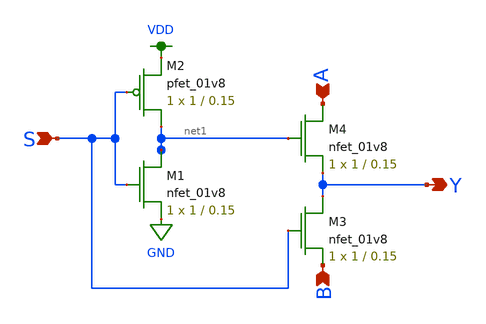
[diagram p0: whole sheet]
** sch_path: schematics/mux.sch
**.subckt mux S A Y B
*.ipin S
*.ipin A
*.opin Y
*.ipin B
XM1 net1 S GND GND sky130_fd_pr__nfet_01v8 L=0.15 W=1 nf=1 ad='int((nf+1)/2) * W/nf * 0.29' as='int((nf+2)/2) * W/nf * 0.29'
+ pd='2*int((nf+1)/2) * (W/nf + 0.29)' ps='2*int((nf+2)/2) * (W/nf + 0.29)' nrd='0.29 / W' nrs='0.29 / W'
+ sa=0 sb=0 sd=0 mult=1 m=1
XM2 net1 S VDD VDD sky130_fd_pr__pfet_01v8 L=0.15 W=1 nf=1 ad='int((nf+1)/2) * W/nf * 0.29' as='int((nf+2)/2) * W/nf * 0.29'
+ pd='2*int((nf+1)/2) * (W/nf + 0.29)' ps='2*int((nf+2)/2) * (W/nf + 0.29)' nrd='0.29 / W' nrs='0.29 / W'
+ sa=0 sb=0 sd=0 mult=1 m=1
XM3 Y S B GND sky130_fd_pr__nfet_01v8 L=0.15 W=1 nf=1 ad='int((nf+1)/2) * W/nf * 0.29' as='int((nf+2)/2) * W/nf * 0.29'
+ pd='2*int((nf+1)/2) * (W/nf + 0.29)' ps='2*int((nf+2)/2) * (W/nf + 0.29)' nrd='0.29 / W' nrs='0.29 / W'
+ sa=0 sb=0 sd=0 mult=1 m=1
XM4 A net1 Y GND sky130_fd_pr__nfet_01v8 L=0.15 W=1 nf=1 ad='int((nf+1)/2) * W/nf * 0.29' as='int((nf+2)/2) * W/nf * 0.29'
+ pd='2*int((nf+1)/2) * (W/nf + 0.29)' ps='2*int((nf+2)/2) * (W/nf + 0.29)' nrd='0.29 / W' nrs='0.29 / W'
+ sa=0 sb=0 sd=0 mult=1 m=1
**.ends
.GLOBAL VDD
.GLOBAL GND
.end
